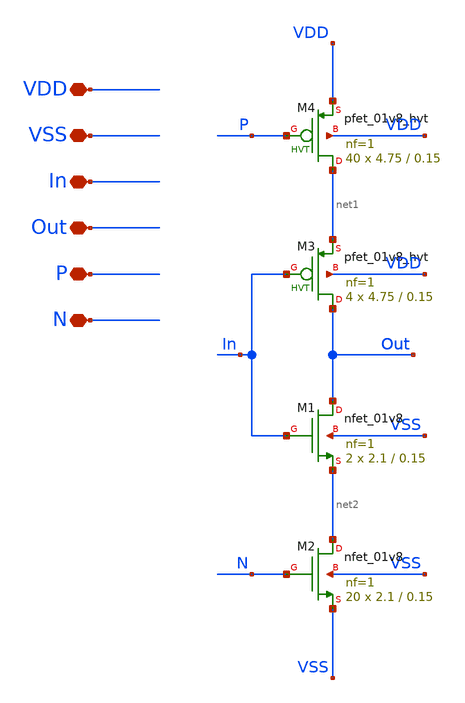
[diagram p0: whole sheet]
** sch_path: HVT/rovcel/rovcel.sch
**.subckt rovcel VDD VSS In Out P N
*.iopin VDD
*.iopin VSS
*.iopin In
*.iopin Out
*.iopin P
*.iopin N
XM3 Out In net1 VDD sky130_fd_pr__pfet_01v8_hvt L=0.15 W=4.75 nf=1 ad='int((nf+1)/2) * W/nf * 0.29' as='int((nf+2)/2) * W/nf * 0.29'
+ pd='2*int((nf+1)/2) * (W/nf + 0.29)' ps='2*int((nf+2)/2) * (W/nf + 0.29)' nrd='0.29 / W' nrs='0.29 / W'
+ sa=0 sb=0 sd=0 mult=4 m=4
XM4 net1 P VDD VDD sky130_fd_pr__pfet_01v8_hvt L=0.15 W=4.75 nf=1 ad='int((nf+1)/2) * W/nf * 0.29' as='int((nf+2)/2) * W/nf * 0.29'
+ pd='2*int((nf+1)/2) * (W/nf + 0.29)' ps='2*int((nf+2)/2) * (W/nf + 0.29)' nrd='0.29 / W' nrs='0.29 / W'
+ sa=0 sb=0 sd=0 mult=40 m=40
XM1 Out In net2 VSS sky130_fd_pr__nfet_01v8 L=0.15 W=2.1 nf=1 ad='int((nf+1)/2) * W/nf * 0.29' as='int((nf+2)/2) * W/nf * 0.29'
+ pd='2*int((nf+1)/2) * (W/nf + 0.29)' ps='2*int((nf+2)/2) * (W/nf + 0.29)' nrd='0.29 / W' nrs='0.29 / W'
+ sa=0 sb=0 sd=0 mult=2 m=2
XM2 net2 N VSS VSS sky130_fd_pr__nfet_01v8 L=0.15 W=2.1 nf=1 ad='int((nf+1)/2) * W/nf * 0.29' as='int((nf+2)/2) * W/nf * 0.29'
+ pd='2*int((nf+1)/2) * (W/nf + 0.29)' ps='2*int((nf+2)/2) * (W/nf + 0.29)' nrd='0.29 / W' nrs='0.29 / W'
+ sa=0 sb=0 sd=0 mult=20 m=20
**.ends
.end
